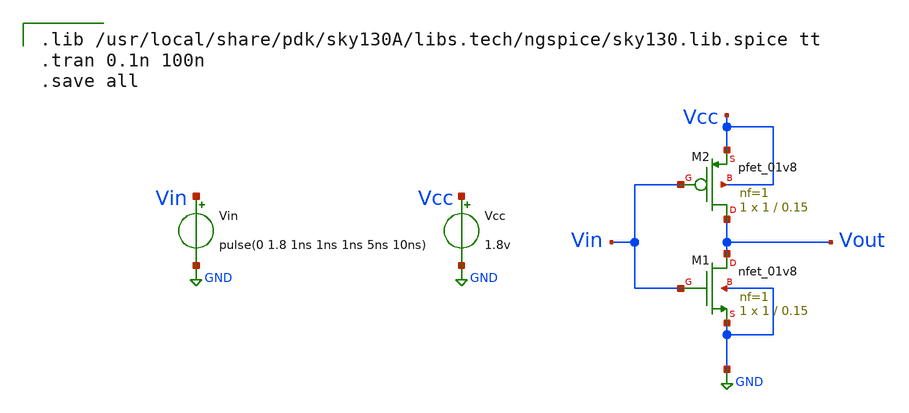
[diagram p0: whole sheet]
** sch_path: first_test/first.sch
**.subckt first
Vin Vin GND pulse(0 1.8 1ns 1ns 1ns 5ns 10ns)
Vcc Vcc GND 1.8v
XM1 Vout Vin GND GND sky130_fd_pr__nfet_01v8 L=0.15 W=1 nf=1 ad='int((nf+1)/2) * W/nf * 0.29' as='int((nf+2)/2) * W/nf * 0.29'
+ pd='2*int((nf+1)/2) * (W/nf + 0.29)' ps='2*int((nf+2)/2) * (W/nf + 0.29)' nrd='0.29 / W' nrs='0.29 / W'
+ sa=0 sb=0 sd=0 mult=1 m=1
XM2 Vout Vin Vcc Vcc sky130_fd_pr__pfet_01v8 L=0.15 W=1 nf=1 ad='int((nf+1)/2) * W/nf * 0.29' as='int((nf+2)/2) * W/nf * 0.29'
+ pd='2*int((nf+1)/2) * (W/nf + 0.29)' ps='2*int((nf+2)/2) * (W/nf + 0.29)' nrd='0.29 / W' nrs='0.29 / W'
+ sa=0 sb=0 sd=0 mult=1 m=1
**** begin user architecture code

.lib /usr/local/share/pdk/sky130A/libs.tech/ngspice/sky130.lib.spice tt
.tran 0.1n 100n
.save all

**** end user architecture code
**.ends
.GLOBAL GND
.end
